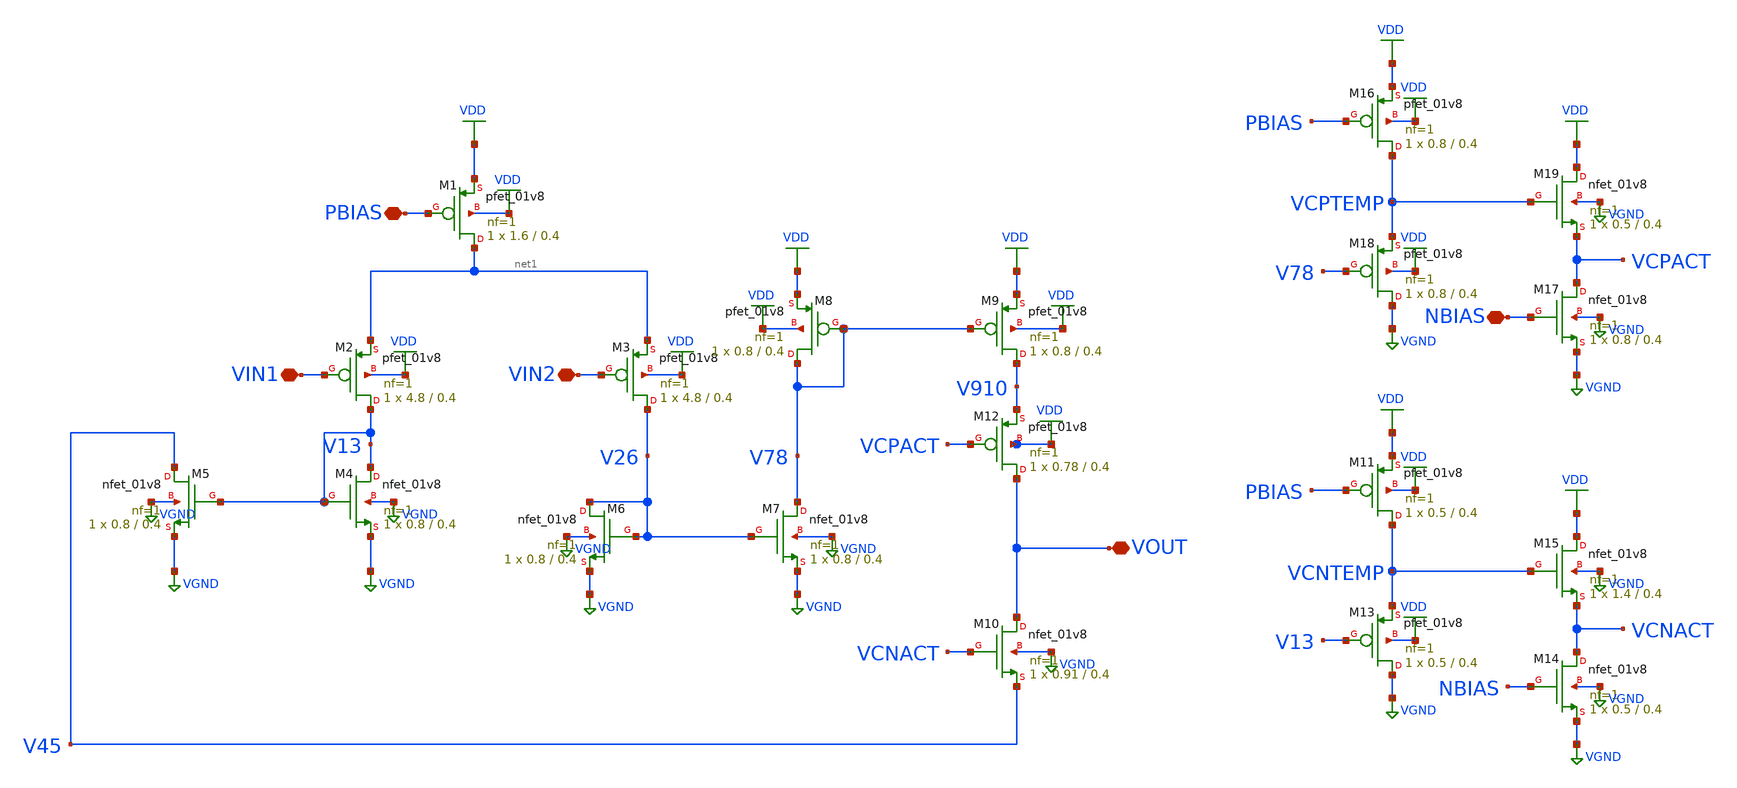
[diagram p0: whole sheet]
** sch_path: project2/design/ota_design.sch
**.subckt ota_design PBIAS VIN1 VIN2 VOUT NBIAS
*.iopin PBIAS
*.iopin VIN1
*.iopin VIN2
*.iopin VOUT
*.iopin NBIAS
XM1 net1 PBIAS VDD VDD sky130_fd_pr__pfet_01v8 L=0.4 W=1.6 nf=1 ad='int((nf+1)/2) * W/nf * 0.29' as='int((nf+2)/2) * W/nf * 0.29'
+ pd='2*int((nf+1)/2) * (W/nf + 0.29)' ps='2*int((nf+2)/2) * (W/nf + 0.29)' nrd='0.29 / W' nrs='0.29 / W'
+ sa=0 sb=0 sd=0 mult=1 m=1
XM2 V13 VIN1 net1 VDD sky130_fd_pr__pfet_01v8 L=0.4 W=4.8 nf=1 ad='int((nf+1)/2) * W/nf * 0.29' as='int((nf+2)/2) * W/nf * 0.29'
+ pd='2*int((nf+1)/2) * (W/nf + 0.29)' ps='2*int((nf+2)/2) * (W/nf + 0.29)' nrd='0.29 / W' nrs='0.29 / W'
+ sa=0 sb=0 sd=0 mult=1 m=1
XM3 V26 VIN2 net1 VDD sky130_fd_pr__pfet_01v8 L=0.4 W=4.8 nf=1 ad='int((nf+1)/2) * W/nf * 0.29' as='int((nf+2)/2) * W/nf * 0.29'
+ pd='2*int((nf+1)/2) * (W/nf + 0.29)' ps='2*int((nf+2)/2) * (W/nf + 0.29)' nrd='0.29 / W' nrs='0.29 / W'
+ sa=0 sb=0 sd=0 mult=1 m=1
XM4 V13 V13 VGND VGND sky130_fd_pr__nfet_01v8 L=0.4 W=0.8 nf=1 ad='int((nf+1)/2) * W/nf * 0.29' as='int((nf+2)/2) * W/nf * 0.29'
+ pd='2*int((nf+1)/2) * (W/nf + 0.29)' ps='2*int((nf+2)/2) * (W/nf + 0.29)' nrd='0.29 / W' nrs='0.29 / W'
+ sa=0 sb=0 sd=0 mult=1 m=1
XM5 V45 V13 VGND VGND sky130_fd_pr__nfet_01v8 L=0.4 W=0.8 nf=1 ad='int((nf+1)/2) * W/nf * 0.29' as='int((nf+2)/2) * W/nf * 0.29'
+ pd='2*int((nf+1)/2) * (W/nf + 0.29)' ps='2*int((nf+2)/2) * (W/nf + 0.29)' nrd='0.29 / W' nrs='0.29 / W'
+ sa=0 sb=0 sd=0 mult=1 m=1
XM6 V26 V26 VGND VGND sky130_fd_pr__nfet_01v8 L=0.4 W=0.8 nf=1 ad='int((nf+1)/2) * W/nf * 0.29' as='int((nf+2)/2) * W/nf * 0.29'
+ pd='2*int((nf+1)/2) * (W/nf + 0.29)' ps='2*int((nf+2)/2) * (W/nf + 0.29)' nrd='0.29 / W' nrs='0.29 / W'
+ sa=0 sb=0 sd=0 mult=1 m=1
XM7 V78 V26 VGND VGND sky130_fd_pr__nfet_01v8 L=0.4 W=0.8 nf=1 ad='int((nf+1)/2) * W/nf * 0.29' as='int((nf+2)/2) * W/nf * 0.29'
+ pd='2*int((nf+1)/2) * (W/nf + 0.29)' ps='2*int((nf+2)/2) * (W/nf + 0.29)' nrd='0.29 / W' nrs='0.29 / W'
+ sa=0 sb=0 sd=0 mult=1 m=1
XM8 V78 V78 VDD VDD sky130_fd_pr__pfet_01v8 L=0.4 W=0.8 nf=1 ad='int((nf+1)/2) * W/nf * 0.29' as='int((nf+2)/2) * W/nf * 0.29'
+ pd='2*int((nf+1)/2) * (W/nf + 0.29)' ps='2*int((nf+2)/2) * (W/nf + 0.29)' nrd='0.29 / W' nrs='0.29 / W'
+ sa=0 sb=0 sd=0 mult=1 m=1
XM9 V910 V78 VDD VDD sky130_fd_pr__pfet_01v8 L=0.4 W=0.8 nf=1 ad='int((nf+1)/2) * W/nf * 0.29' as='int((nf+2)/2) * W/nf * 0.29'
+ pd='2*int((nf+1)/2) * (W/nf + 0.29)' ps='2*int((nf+2)/2) * (W/nf + 0.29)' nrd='0.29 / W' nrs='0.29 / W'
+ sa=0 sb=0 sd=0 mult=1 m=1
XM10 VOUT VCNACT V45 VGND sky130_fd_pr__nfet_01v8 L=0.4 W=0.91 nf=1 ad='int((nf+1)/2) * W/nf * 0.29'
+ as='int((nf+2)/2) * W/nf * 0.29' pd='2*int((nf+1)/2) * (W/nf + 0.29)' ps='2*int((nf+2)/2) * (W/nf + 0.29)'
+ nrd='0.29 / W' nrs='0.29 / W' sa=0 sb=0 sd=0 mult=1 m=1
XM12 VOUT VCPACT V910 VDD sky130_fd_pr__pfet_01v8 L=0.4 W=0.78 nf=1 ad='int((nf+1)/2) * W/nf * 0.29'
+ as='int((nf+2)/2) * W/nf * 0.29' pd='2*int((nf+1)/2) * (W/nf + 0.29)' ps='2*int((nf+2)/2) * (W/nf + 0.29)'
+ nrd='0.29 / W' nrs='0.29 / W' sa=0 sb=0 sd=0 mult=1 m=1
XM11 VCNTEMP PBIAS VDD VDD sky130_fd_pr__pfet_01v8 L=0.4 W=0.5 nf=1 ad='int((nf+1)/2) * W/nf * 0.29'
+ as='int((nf+2)/2) * W/nf * 0.29' pd='2*int((nf+1)/2) * (W/nf + 0.29)' ps='2*int((nf+2)/2) * (W/nf + 0.29)'
+ nrd='0.29 / W' nrs='0.29 / W' sa=0 sb=0 sd=0 mult=1 m=1
XM14 VCNACT NBIAS VGND VGND sky130_fd_pr__nfet_01v8 L=0.4 W=0.5 nf=1 ad='int((nf+1)/2) * W/nf * 0.29'
+ as='int((nf+2)/2) * W/nf * 0.29' pd='2*int((nf+1)/2) * (W/nf + 0.29)' ps='2*int((nf+2)/2) * (W/nf + 0.29)'
+ nrd='0.29 / W' nrs='0.29 / W' sa=0 sb=0 sd=0 mult=1 m=1
XM13 VGND V13 VCNTEMP VDD sky130_fd_pr__pfet_01v8 L=0.4 W=0.5 nf=1 ad='int((nf+1)/2) * W/nf * 0.29' as='int((nf+2)/2) * W/nf * 0.29'
+ pd='2*int((nf+1)/2) * (W/nf + 0.29)' ps='2*int((nf+2)/2) * (W/nf + 0.29)' nrd='0.29 / W' nrs='0.29 / W'
+ sa=0 sb=0 sd=0 mult=1 m=1
XM15 VDD VCNTEMP VCNACT VGND sky130_fd_pr__nfet_01v8 L=0.4 W=1.4 nf=1 ad='int((nf+1)/2) * W/nf * 0.29'
+ as='int((nf+2)/2) * W/nf * 0.29' pd='2*int((nf+1)/2) * (W/nf + 0.29)' ps='2*int((nf+2)/2) * (W/nf + 0.29)'
+ nrd='0.29 / W' nrs='0.29 / W' sa=0 sb=0 sd=0 mult=1 m=1
XM16 VCPTEMP PBIAS VDD VDD sky130_fd_pr__pfet_01v8 L=0.4 W=0.8 nf=1 ad='int((nf+1)/2) * W/nf * 0.29'
+ as='int((nf+2)/2) * W/nf * 0.29' pd='2*int((nf+1)/2) * (W/nf + 0.29)' ps='2*int((nf+2)/2) * (W/nf + 0.29)'
+ nrd='0.29 / W' nrs='0.29 / W' sa=0 sb=0 sd=0 mult=1 m=1
XM17 VCPACT NBIAS VGND VGND sky130_fd_pr__nfet_01v8 L=0.4 W=0.8 nf=1 ad='int((nf+1)/2) * W/nf * 0.29'
+ as='int((nf+2)/2) * W/nf * 0.29' pd='2*int((nf+1)/2) * (W/nf + 0.29)' ps='2*int((nf+2)/2) * (W/nf + 0.29)'
+ nrd='0.29 / W' nrs='0.29 / W' sa=0 sb=0 sd=0 mult=1 m=1
XM18 VGND V78 VCPTEMP VDD sky130_fd_pr__pfet_01v8 L=0.4 W=0.8 nf=1 ad='int((nf+1)/2) * W/nf * 0.29' as='int((nf+2)/2) * W/nf * 0.29'
+ pd='2*int((nf+1)/2) * (W/nf + 0.29)' ps='2*int((nf+2)/2) * (W/nf + 0.29)' nrd='0.29 / W' nrs='0.29 / W'
+ sa=0 sb=0 sd=0 mult=1 m=1
XM19 VDD VCPTEMP VCPACT VGND sky130_fd_pr__nfet_01v8 L=0.4 W=0.5 nf=1 ad='int((nf+1)/2) * W/nf * 0.29'
+ as='int((nf+2)/2) * W/nf * 0.29' pd='2*int((nf+1)/2) * (W/nf + 0.29)' ps='2*int((nf+2)/2) * (W/nf + 0.29)'
+ nrd='0.29 / W' nrs='0.29 / W' sa=0 sb=0 sd=0 mult=1 m=1
**.ends
.GLOBAL VDD
.GLOBAL VGND
.end
